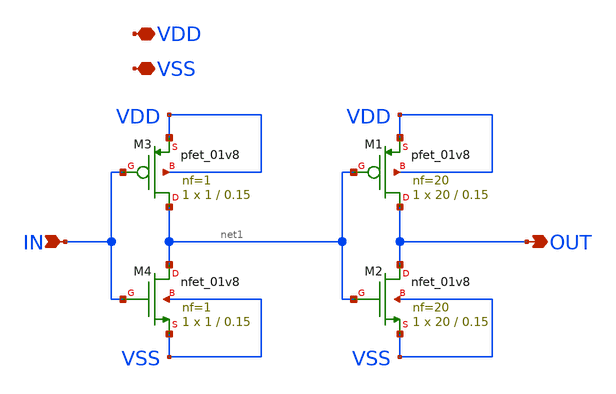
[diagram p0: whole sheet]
** sch_path: xschem/inverter.sch
**.subckt inverter VDD VSS IN OUT
*.iopin VDD
*.iopin VSS
*.ipin IN
*.opin OUT
XM1 OUT net1 VDD VDD sky130_fd_pr__pfet_01v8 L=0.15 W=20 nf=20 ad='int((nf+1)/2) * W/nf * 0.29' as='int((nf+2)/2) * W/nf * 0.29'
+ pd='2*int((nf+1)/2) * (W/nf + 0.29)' ps='2*int((nf+2)/2) * (W/nf + 0.29)' nrd='0.29 / W' nrs='0.29 / W'
+ sa=0 sb=0 sd=0 mult=1 m=1
XM2 OUT net1 VSS VSS sky130_fd_pr__nfet_01v8 L=0.15 W=20 nf=20 ad='int((nf+1)/2) * W/nf * 0.29' as='int((nf+2)/2) * W/nf * 0.29'
+ pd='2*int((nf+1)/2) * (W/nf + 0.29)' ps='2*int((nf+2)/2) * (W/nf + 0.29)' nrd='0.29 / W' nrs='0.29 / W'
+ sa=0 sb=0 sd=0 mult=1 m=1
XM3 net1 IN VDD VDD sky130_fd_pr__pfet_01v8 L=0.15 W=1 nf=1 ad='int((nf+1)/2) * W/nf * 0.29' as='int((nf+2)/2) * W/nf * 0.29'
+ pd='2*int((nf+1)/2) * (W/nf + 0.29)' ps='2*int((nf+2)/2) * (W/nf + 0.29)' nrd='0.29 / W' nrs='0.29 / W'
+ sa=0 sb=0 sd=0 mult=1 m=1
XM4 net1 IN VSS VSS sky130_fd_pr__nfet_01v8 L=0.15 W=1 nf=1 ad='int((nf+1)/2) * W/nf * 0.29' as='int((nf+2)/2) * W/nf * 0.29'
+ pd='2*int((nf+1)/2) * (W/nf + 0.29)' ps='2*int((nf+2)/2) * (W/nf + 0.29)' nrd='0.29 / W' nrs='0.29 / W'
+ sa=0 sb=0 sd=0 mult=1 m=1
**.ends
.end
